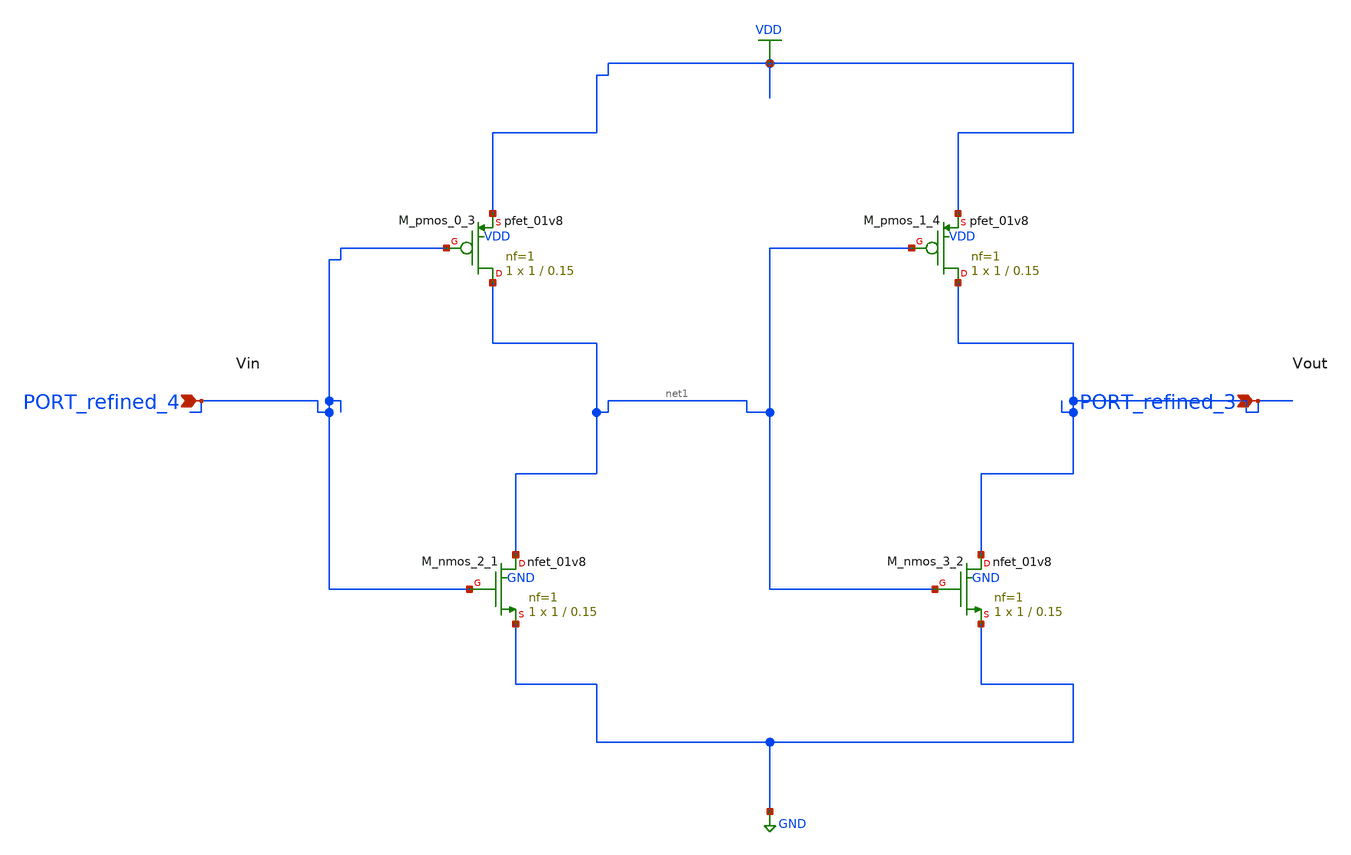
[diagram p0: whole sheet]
** sch_path: schematics/SchemGen/10_1038_s41598-025-17286-6_08_001.sch
**.subckt 10_1038_s41598-025-17286-6_08_001 PORT_refined_4 PORT_refined_3
*.ipin PORT_refined_4
*.ipin PORT_refined_3
XM_nmos_2_1 net1 PORT_refined_4 GND GND sky130_fd_pr__nfet_01v8 L=0.15 W=1 nf=1 ad='int((1 + 1)/2) * 1 / 1 * 0.29'
+ as='int((1 + 2)/2) * 1 / 1 * 0.29' pd='2*int((1 + 1)/2) * (1 / 1 + 0.29)' ps='2*int((1 + 2)/2) * (1 / 1 + 0.29)'
+ nrd='0.29 / 1 ' nrs='0.29 / 1 ' sa=0 sb=0 sd=0 mult=1 m=1
XM_nmos_3_2 PORT_refined_3 net1 GND GND sky130_fd_pr__nfet_01v8 L=0.15 W=1 nf=1 ad='int((1 + 1)/2) * 1 / 1 * 0.29'
+ as='int((1 + 2)/2) * 1 / 1 * 0.29' pd='2*int((1 + 1)/2) * (1 / 1 + 0.29)' ps='2*int((1 + 2)/2) * (1 / 1 + 0.29)'
+ nrd='0.29 / 1 ' nrs='0.29 / 1 ' sa=0 sb=0 sd=0 mult=1 m=1
XM_pmos_0_3 net1 PORT_refined_4 VDD VDD sky130_fd_pr__pfet_01v8 L=0.15 W=1 nf=1 ad='int((1 + 1)/2) * 1 / 1 * 0.29'
+ as='int((1 + 2)/2) * 1 / 1 * 0.29' pd='2*int((1 + 1)/2) * (1 / 1 + 0.29)' ps='2*int((1 + 2)/2) * (1 / 1 + 0.29)'
+ nrd='0.29 / 1 ' nrs='0.29 / 1 ' sa=0 sb=0 sd=0 mult=1 m=1
XM_pmos_1_4 PORT_refined_3 net1 VDD VDD sky130_fd_pr__pfet_01v8 L=0.15 W=1 nf=1 ad='int((1 + 1)/2) * 1 / 1 * 0.29'
+ as='int((1 + 2)/2) * 1 / 1 * 0.29' pd='2*int((1 + 1)/2) * (1 / 1 + 0.29)' ps='2*int((1 + 2)/2) * (1 / 1 + 0.29)'
+ nrd='0.29 / 1 ' nrs='0.29 / 1 ' sa=0 sb=0 sd=0 mult=1 m=1
**.ends
.GLOBAL GND
.GLOBAL VDD
.end
